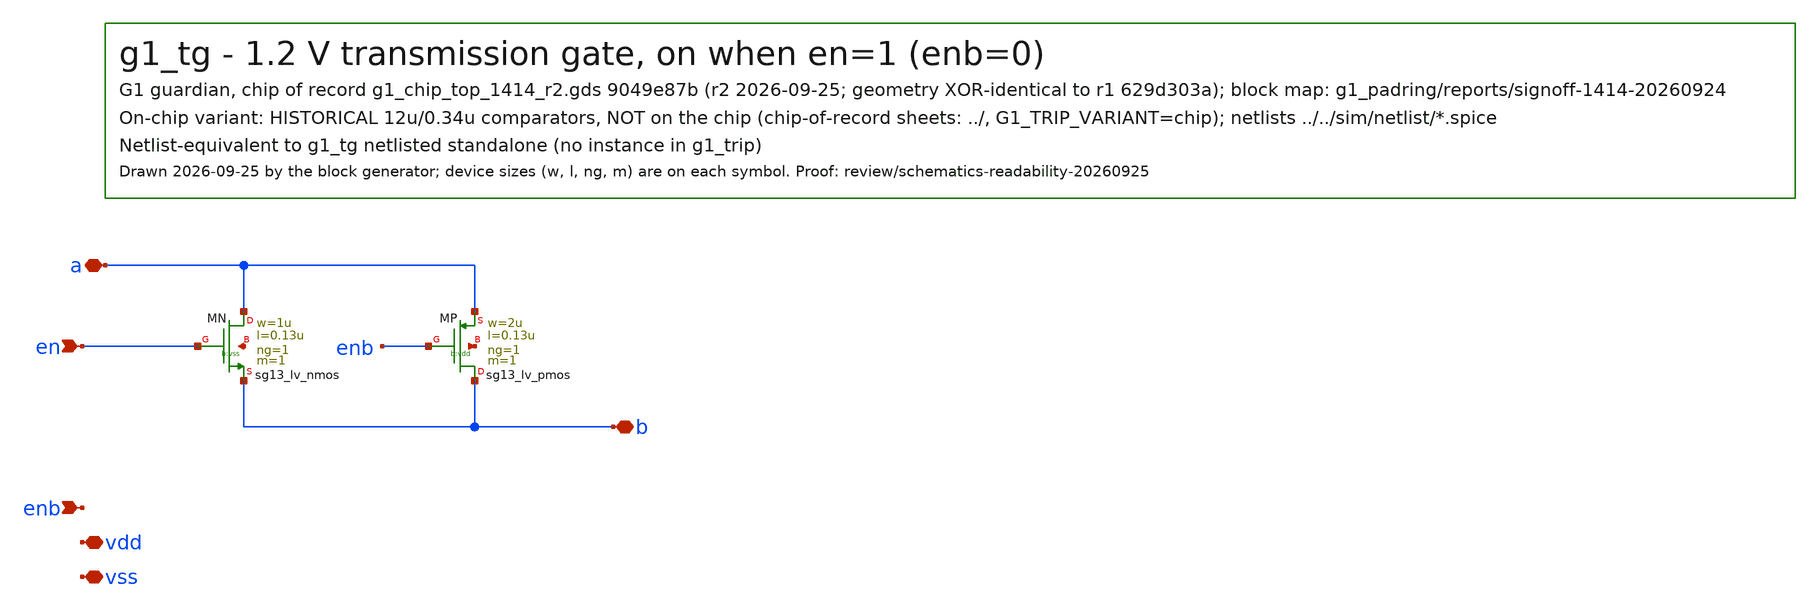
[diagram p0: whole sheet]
** sch_path: designs/g1-guardian/blocks/g1_trip/schematic/historical_12u034/g1_tg.sch
**.subckt g1_tg en enb a b vdd vss
*.ipin en
*.ipin enb
*.iopin a
*.iopin b
*.iopin vdd
*.iopin vss
XMN a en b vss sg13_lv_nmos w=1u l=0.13u ng=1 m=1 mm_ok=1
XMP b enb a vdd sg13_lv_pmos w=2u l=0.13u ng=1 m=1 mm_ok=1
**.ends
.end
